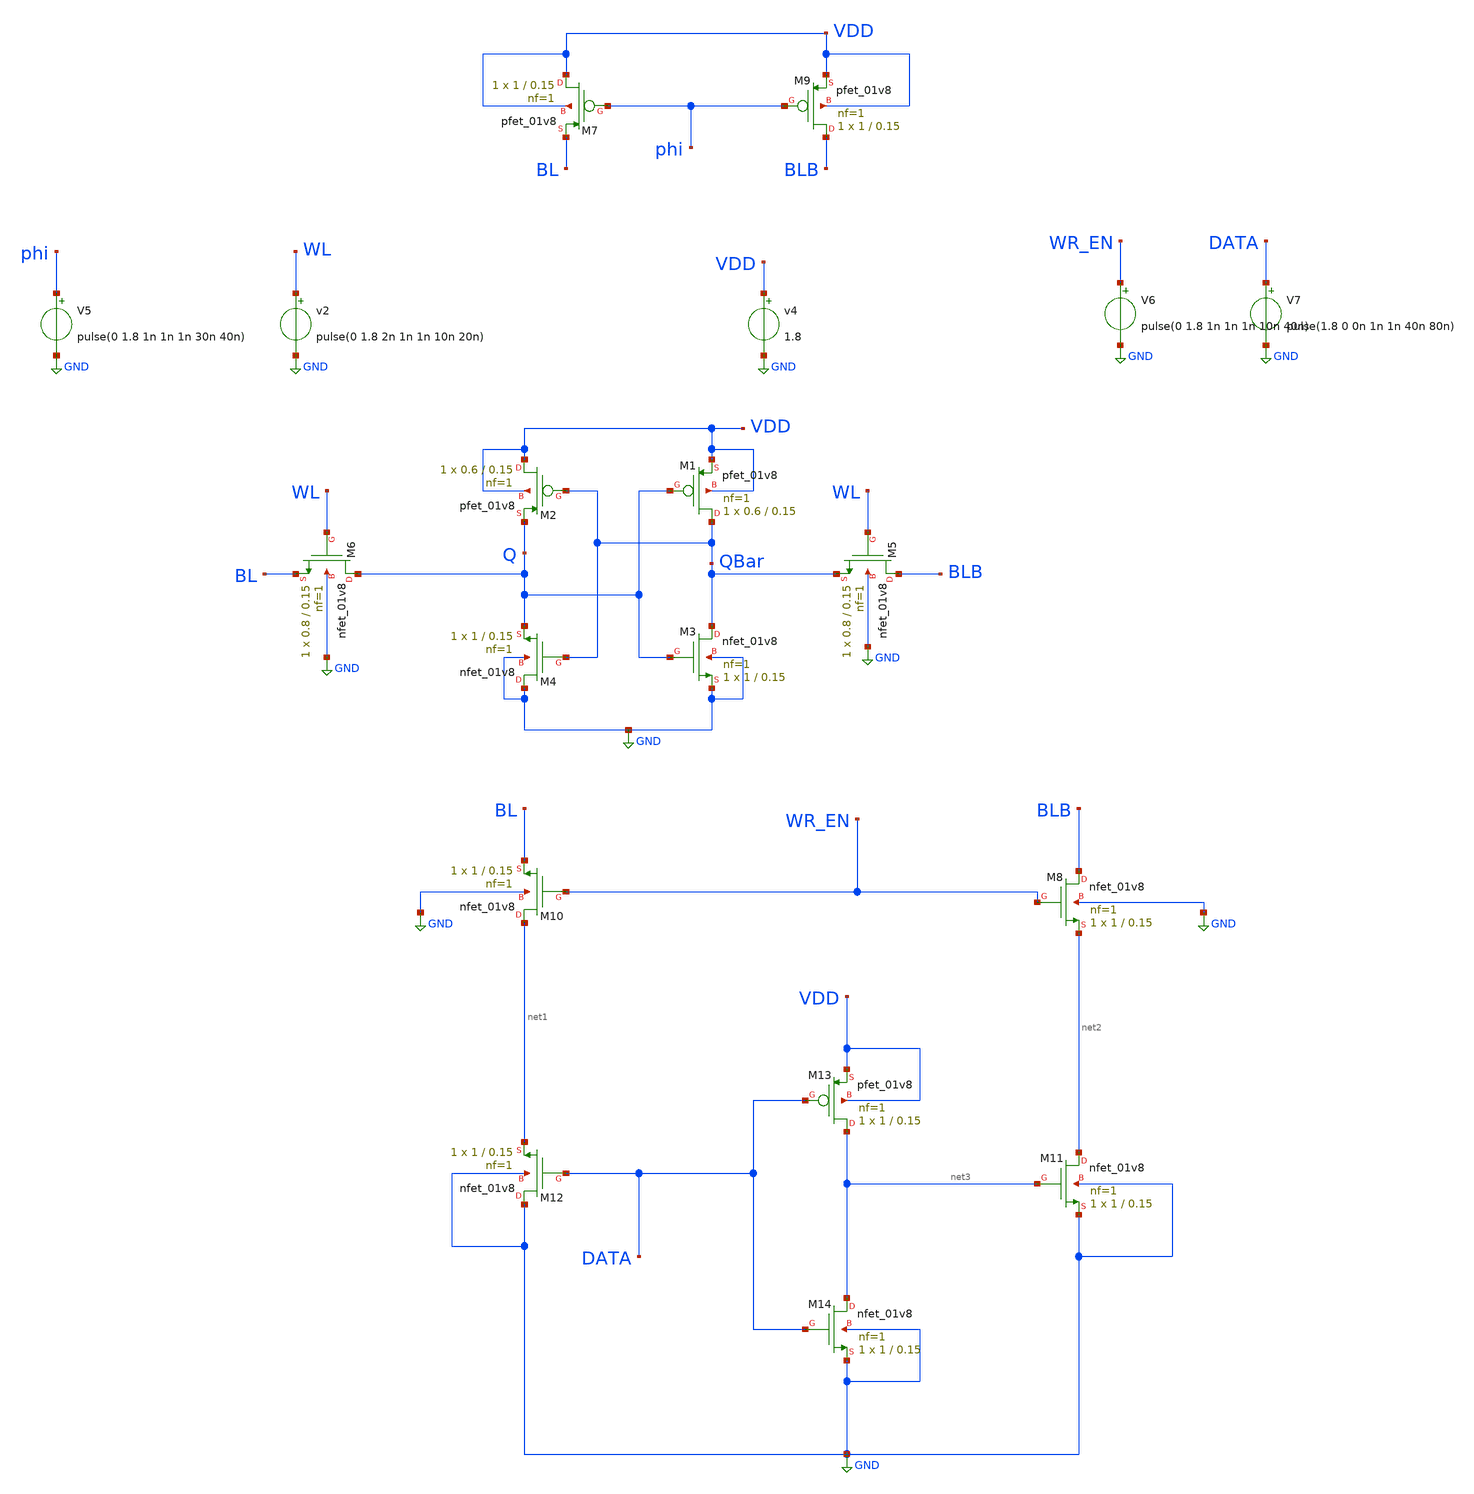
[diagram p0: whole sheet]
** sch_path: sramcell.sch
**.subckt sramcell
XM1 QBar Q VDD VDD sky130_fd_pr__pfet_01v8 L=0.15 W=0.6 nf=1 ad='int((nf+1)/2) * W/nf * 0.29' as='int((nf+2)/2) * W/nf * 0.29'
+ pd='2*int((nf+1)/2) * (W/nf + 0.29)' ps='2*int((nf+2)/2) * (W/nf + 0.29)' nrd='0.29 / W' nrs='0.29 / W'
+ sa=0 sb=0 sd=0 mult=1 m=1
XM2 VDD QBar Q VDD sky130_fd_pr__pfet_01v8 L=0.15 W=0.6 nf=1 ad='int((nf+1)/2) * W/nf * 0.29' as='int((nf+2)/2) * W/nf * 0.29'
+ pd='2*int((nf+1)/2) * (W/nf + 0.29)' ps='2*int((nf+2)/2) * (W/nf + 0.29)' nrd='0.29 / W' nrs='0.29 / W'
+ sa=0 sb=0 sd=0 mult=1 m=1
XM3 QBar Q GND GND sky130_fd_pr__nfet_01v8 L=0.15 W=1 nf=1 ad='int((nf+1)/2) * W/nf * 0.29' as='int((nf+2)/2) * W/nf * 0.29'
+ pd='2*int((nf+1)/2) * (W/nf + 0.29)' ps='2*int((nf+2)/2) * (W/nf + 0.29)' nrd='0.29 / W' nrs='0.29 / W'
+ sa=0 sb=0 sd=0 mult=1 m=1
XM4 GND QBar Q GND sky130_fd_pr__nfet_01v8 L=0.15 W=1 nf=1 ad='int((nf+1)/2) * W/nf * 0.29' as='int((nf+2)/2) * W/nf * 0.29'
+ pd='2*int((nf+1)/2) * (W/nf + 0.29)' ps='2*int((nf+2)/2) * (W/nf + 0.29)' nrd='0.29 / W' nrs='0.29 / W'
+ sa=0 sb=0 sd=0 mult=1 m=1
XM5 BLB WL QBar GND sky130_fd_pr__nfet_01v8 L=0.15 W=0.8 nf=1 ad='int((nf+1)/2) * W/nf * 0.29' as='int((nf+2)/2) * W/nf * 0.29'
+ pd='2*int((nf+1)/2) * (W/nf + 0.29)' ps='2*int((nf+2)/2) * (W/nf + 0.29)' nrd='0.29 / W' nrs='0.29 / W'
+ sa=0 sb=0 sd=0 mult=1 m=1
XM6 Q WL BL GND sky130_fd_pr__nfet_01v8 L=0.15 W=0.8 nf=1 ad='int((nf+1)/2) * W/nf * 0.29' as='int((nf+2)/2) * W/nf * 0.29'
+ pd='2*int((nf+1)/2) * (W/nf + 0.29)' ps='2*int((nf+2)/2) * (W/nf + 0.29)' nrd='0.29 / W' nrs='0.29 / W'
+ sa=0 sb=0 sd=0 mult=1 m=1
v4 VDD GND 1.8
v2 WL GND pulse(0 1.8 2n 1n 1n 10n 20n)
XM9 BLB phi VDD VDD sky130_fd_pr__pfet_01v8 L=0.15 W=1 nf=1 ad='int((nf+1)/2) * W/nf * 0.29' as='int((nf+2)/2) * W/nf * 0.29'
+ pd='2*int((nf+1)/2) * (W/nf + 0.29)' ps='2*int((nf+2)/2) * (W/nf + 0.29)' nrd='0.29 / W' nrs='0.29 / W'
+ sa=0 sb=0 sd=0 mult=1 m=1
XM7 VDD phi BL VDD sky130_fd_pr__pfet_01v8 L=0.15 W=1 nf=1 ad='int((nf+1)/2) * W/nf * 0.29' as='int((nf+2)/2) * W/nf * 0.29'
+ pd='2*int((nf+1)/2) * (W/nf + 0.29)' ps='2*int((nf+2)/2) * (W/nf + 0.29)' nrd='0.29 / W' nrs='0.29 / W'
+ sa=0 sb=0 sd=0 mult=1 m=1
V5 phi GND pulse(0 1.8 1n 1n 1n 30n 40n)
XM8 BLB WR_EN net2 GND sky130_fd_pr__nfet_01v8 L=0.15 W=1 nf=1 ad='int((nf+1)/2) * W/nf * 0.29' as='int((nf+2)/2) * W/nf * 0.29'
+ pd='2*int((nf+1)/2) * (W/nf + 0.29)' ps='2*int((nf+2)/2) * (W/nf + 0.29)' nrd='0.29 / W' nrs='0.29 / W'
+ sa=0 sb=0 sd=0 mult=1 m=1
XM10 net1 WR_EN BL GND sky130_fd_pr__nfet_01v8 L=0.15 W=1 nf=1 ad='int((nf+1)/2) * W/nf * 0.29' as='int((nf+2)/2) * W/nf * 0.29'
+ pd='2*int((nf+1)/2) * (W/nf + 0.29)' ps='2*int((nf+2)/2) * (W/nf + 0.29)' nrd='0.29 / W' nrs='0.29 / W'
+ sa=0 sb=0 sd=0 mult=1 m=1
XM11 net2 net3 GND GND sky130_fd_pr__nfet_01v8 L=0.15 W=1 nf=1 ad='int((nf+1)/2) * W/nf * 0.29' as='int((nf+2)/2) * W/nf * 0.29'
+ pd='2*int((nf+1)/2) * (W/nf + 0.29)' ps='2*int((nf+2)/2) * (W/nf + 0.29)' nrd='0.29 / W' nrs='0.29 / W'
+ sa=0 sb=0 sd=0 mult=1 m=1
XM12 GND DATA net1 GND sky130_fd_pr__nfet_01v8 L=0.15 W=1 nf=1 ad='int((nf+1)/2) * W/nf * 0.29' as='int((nf+2)/2) * W/nf * 0.29'
+ pd='2*int((nf+1)/2) * (W/nf + 0.29)' ps='2*int((nf+2)/2) * (W/nf + 0.29)' nrd='0.29 / W' nrs='0.29 / W'
+ sa=0 sb=0 sd=0 mult=1 m=1
XM13 net3 DATA VDD VDD sky130_fd_pr__pfet_01v8 L=0.15 W=1 nf=1 ad='int((nf+1)/2) * W/nf * 0.29' as='int((nf+2)/2) * W/nf * 0.29'
+ pd='2*int((nf+1)/2) * (W/nf + 0.29)' ps='2*int((nf+2)/2) * (W/nf + 0.29)' nrd='0.29 / W' nrs='0.29 / W'
+ sa=0 sb=0 sd=0 mult=1 m=1
XM14 net3 DATA GND GND sky130_fd_pr__nfet_01v8 L=0.15 W=1 nf=1 ad='int((nf+1)/2) * W/nf * 0.29' as='int((nf+2)/2) * W/nf * 0.29'
+ pd='2*int((nf+1)/2) * (W/nf + 0.29)' ps='2*int((nf+2)/2) * (W/nf + 0.29)' nrd='0.29 / W' nrs='0.29 / W'
+ sa=0 sb=0 sd=0 mult=1 m=1
V6 WR_EN GND pulse(0 1.8 1n 1n 1n 10n 40n)
V7 DATA GND pulse(1.8 0 0n 1n 1n 40n 80n)
**** begin user architecture code

.lib /home/avs/whyRD_eda_bundle/open_pdks/sky130/sky130A/libs.tech/ngspice/sky130.lib.spice tt
.tran 0.1n 200n
.control
run
plot v(Q), v(QBar)+2, v(BL)+4,v(BLB)+6, v(WL)+8,v(phi)+10,v(WR_EN)+12,v(DATA)+14
.endc
.save all

**** end user architecture code
**.ends
.GLOBAL GND
.end
